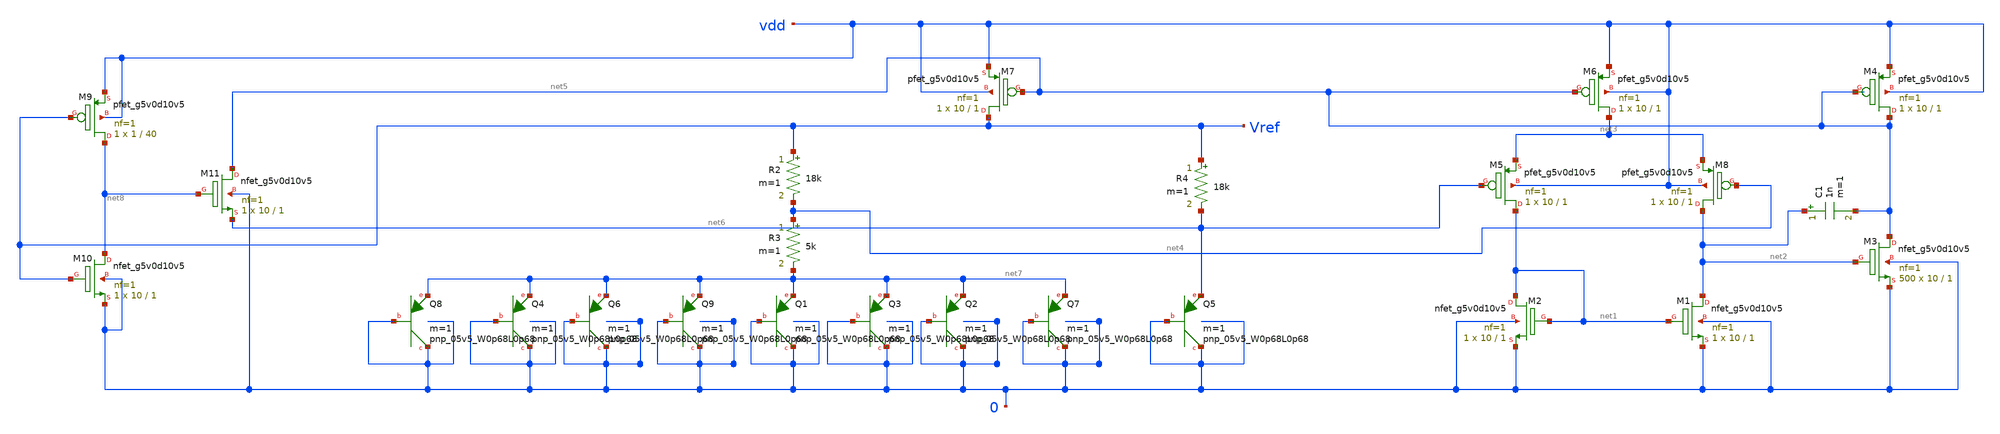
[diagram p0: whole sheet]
** sch_path: Bandgap/My Design/Schematics/Bandgap_opamp.sch
**.subckt Bandgap_opamp
XQ3 0 0 net7 sky130_fd_pr__pnp_05v5_W0p68L0p68 m=1
C1 net2 net5 1n m=1
XQ5 0 0 net6 sky130_fd_pr__pnp_05v5_W0p68L0p68 m=1
R2 Vref net4 18k m=1
R3 net4 net7 5k m=1
R4 Vref net6 18k m=1
XQ9 0 0 net7 sky130_fd_pr__pnp_05v5_W0p68L0p68 m=1
XQ1 0 0 net7 sky130_fd_pr__pnp_05v5_W0p68L0p68 m=1
XQ2 0 0 net7 sky130_fd_pr__pnp_05v5_W0p68L0p68 m=1
XQ4 0 0 net7 sky130_fd_pr__pnp_05v5_W0p68L0p68 m=1
XQ6 0 0 net7 sky130_fd_pr__pnp_05v5_W0p68L0p68 m=1
XQ7 0 0 net7 sky130_fd_pr__pnp_05v5_W0p68L0p68 m=1
XQ8 0 0 net7 sky130_fd_pr__pnp_05v5_W0p68L0p68 m=1
XM1 net2 net1 0 0 sky130_fd_pr__nfet_g5v0d10v5 L=1 W=10 nf=1 ad='int((nf+1)/2) * W/nf * 0.29' as='int((nf+2)/2) * W/nf * 0.29'
+ pd='2*int((nf+1)/2) * (W/nf + 0.29)' ps='2*int((nf+2)/2) * (W/nf + 0.29)' nrd='0.29 / W' nrs='0.29 / W'
+ sa=0 sb=0 sd=0 mult=1 m=1
XM2 net1 net1 0 0 sky130_fd_pr__nfet_g5v0d10v5 L=1 W=10 nf=1 ad='int((nf+1)/2) * W/nf * 0.29' as='int((nf+2)/2) * W/nf * 0.29'
+ pd='2*int((nf+1)/2) * (W/nf + 0.29)' ps='2*int((nf+2)/2) * (W/nf + 0.29)' nrd='0.29 / W' nrs='0.29 / W'
+ sa=0 sb=0 sd=0 mult=1 m=1
XM3 net5 net2 0 0 sky130_fd_pr__nfet_g5v0d10v5 L=1 W=10 nf=1 ad='int((nf+1)/2) * W/nf * 0.29' as='int((nf+2)/2) * W/nf * 0.29'
+ pd='2*int((nf+1)/2) * (W/nf + 0.29)' ps='2*int((nf+2)/2) * (W/nf + 0.29)' nrd='0.29 / W' nrs='0.29 / W'
+ sa=0 sb=0 sd=0 mult=500 m=500
XM4 net5 net5 vdd vdd sky130_fd_pr__pfet_g5v0d10v5 L=1 W=10 nf=1 ad='int((nf+1)/2) * W/nf * 0.29' as='int((nf+2)/2) * W/nf * 0.29'
+ pd='2*int((nf+1)/2) * (W/nf + 0.29)' ps='2*int((nf+2)/2) * (W/nf + 0.29)' nrd='0.29 / W' nrs='0.29 / W'
+ sa=0 sb=0 sd=0 mult=1 m=1
XM5 net1 net6 net3 vdd sky130_fd_pr__pfet_g5v0d10v5 L=1 W=10 nf=1 ad='int((nf+1)/2) * W/nf * 0.29' as='int((nf+2)/2) * W/nf * 0.29'
+ pd='2*int((nf+1)/2) * (W/nf + 0.29)' ps='2*int((nf+2)/2) * (W/nf + 0.29)' nrd='0.29 / W' nrs='0.29 / W'
+ sa=0 sb=0 sd=0 mult=1 m=1
XM6 net3 net5 vdd vdd sky130_fd_pr__pfet_g5v0d10v5 L=1 W=10 nf=1 ad='int((nf+1)/2) * W/nf * 0.29' as='int((nf+2)/2) * W/nf * 0.29'
+ pd='2*int((nf+1)/2) * (W/nf + 0.29)' ps='2*int((nf+2)/2) * (W/nf + 0.29)' nrd='0.29 / W' nrs='0.29 / W'
+ sa=0 sb=0 sd=0 mult=1 m=1
XM7 Vref net5 vdd vdd sky130_fd_pr__pfet_g5v0d10v5 L=1 W=10 nf=1 ad='int((nf+1)/2) * W/nf * 0.29' as='int((nf+2)/2) * W/nf * 0.29'
+ pd='2*int((nf+1)/2) * (W/nf + 0.29)' ps='2*int((nf+2)/2) * (W/nf + 0.29)' nrd='0.29 / W' nrs='0.29 / W'
+ sa=0 sb=0 sd=0 mult=1 m=1
XM8 net2 net4 net3 vdd sky130_fd_pr__pfet_g5v0d10v5 L=1 W=10 nf=1 ad='int((nf+1)/2) * W/nf * 0.29' as='int((nf+2)/2) * W/nf * 0.29'
+ pd='2*int((nf+1)/2) * (W/nf + 0.29)' ps='2*int((nf+2)/2) * (W/nf + 0.29)' nrd='0.29 / W' nrs='0.29 / W'
+ sa=0 sb=0 sd=0 mult=1 m=1
XM9 net8 Vref vdd vdd sky130_fd_pr__pfet_g5v0d10v5 L=40 W=1 nf=1 ad='int((nf+1)/2) * W/nf * 0.29' as='int((nf+2)/2) * W/nf * 0.29'
+ pd='2*int((nf+1)/2) * (W/nf + 0.29)' ps='2*int((nf+2)/2) * (W/nf + 0.29)' nrd='0.29 / W' nrs='0.29 / W'
+ sa=0 sb=0 sd=0 mult=1 m=1
XM10 net8 Vref 0 0 sky130_fd_pr__nfet_g5v0d10v5 L=1 W=10 nf=1 ad='int((nf+1)/2) * W/nf * 0.29' as='int((nf+2)/2) * W/nf * 0.29'
+ pd='2*int((nf+1)/2) * (W/nf + 0.29)' ps='2*int((nf+2)/2) * (W/nf + 0.29)' nrd='0.29 / W' nrs='0.29 / W'
+ sa=0 sb=0 sd=0 mult=1 m=1
XM11 net5 net8 net6 0 sky130_fd_pr__nfet_g5v0d10v5 L=1 W=10 nf=1 ad='int((nf+1)/2) * W/nf * 0.29' as='int((nf+2)/2) * W/nf * 0.29'
+ pd='2*int((nf+1)/2) * (W/nf + 0.29)' ps='2*int((nf+2)/2) * (W/nf + 0.29)' nrd='0.29 / W' nrs='0.29 / W'
+ sa=0 sb=0 sd=0 mult=1 m=1
**** begin user architecture code

.include $::SKYWATER_MODELS/cells/nfet_01v8/sky130_fd_pr__nfet_01v8__tt.corner.spice
.include $::SKYWATER_MODELS/cells/nfet_01v8_lvt/sky130_fd_pr__nfet_01v8_lvt__tt.corner.spice
.include $::SKYWATER_MODELS/cells/pfet_01v8/sky130_fd_pr__pfet_01v8__tt.corner.spice
.include $::SKYWATER_MODELS/cells/nfet_03v3_nvt/sky130_fd_pr__nfet_03v3_nvt__tt.corner.spice
.include $::SKYWATER_MODELS/cells/nfet_05v0_nvt/sky130_fd_pr__nfet_05v0_nvt__tt.corner.spice
.include $::SKYWATER_MODELS/cells/esd_nfet_01v8/sky130_fd_pr__esd_nfet_01v8__tt.corner.spice
.include $::SKYWATER_MODELS/cells/pfet_01v8_lvt/sky130_fd_pr__pfet_01v8_lvt__tt.corner.spice
.include $::SKYWATER_MODELS/cells/pfet_01v8_hvt/sky130_fd_pr__pfet_01v8_hvt__tt.corner.spice
.include $::SKYWATER_MODELS/cells/esd_pfet_g5v0d10v5/sky130_fd_pr__esd_pfet_g5v0d10v5__tt.corner.spice
.include $::SKYWATER_MODELS/cells/pfet_g5v0d10v5/sky130_fd_pr__pfet_g5v0d10v5__tt.corner.spice
.include $::SKYWATER_MODELS/cells/pfet_g5v0d16v0/sky130_fd_pr__pfet_g5v0d16v0__tt.corner.spice
.include $::SKYWATER_MODELS/cells/nfet_g5v0d10v5/sky130_fd_pr__nfet_g5v0d10v5__tt.corner.spice
.include $::SKYWATER_MODELS/cells/nfet_g5v0d16v0/sky130_fd_pr__nfet_g5v0d16v0__tt_discrete.corner.spice
.include $::SKYWATER_MODELS/cells/esd_nfet_g5v0d10v5/sky130_fd_pr__esd_nfet_g5v0d10v5__tt.corner.spice
.include $::SKYWATER_MODELS/models/corners/tt/nonfet.spice
* Mismatch parameters
.include $::SKYWATER_MODELS/cells/nfet_01v8/sky130_fd_pr__nfet_01v8__mismatch.corner.spice
.include $::SKYWATER_MODELS/cells/pfet_01v8/sky130_fd_pr__pfet_01v8__mismatch.corner.spice
.include $::SKYWATER_MODELS/cells/nfet_01v8_lvt/sky130_fd_pr__nfet_01v8_lvt__mismatch.corner.spice
.include $::SKYWATER_MODELS/cells/pfet_01v8_lvt/sky130_fd_pr__pfet_01v8_lvt__mismatch.corner.spice
.include $::SKYWATER_MODELS/cells/pfet_01v8_hvt/sky130_fd_pr__pfet_01v8_hvt__mismatch.corner.spice
.include $::SKYWATER_MODELS/cells/nfet_g5v0d10v5/sky130_fd_pr__nfet_g5v0d10v5__mismatch.corner.spice
.include $::SKYWATER_MODELS/cells/pfet_g5v0d10v5/sky130_fd_pr__pfet_g5v0d10v5__mismatch.corner.spice
.include $::SKYWATER_MODELS/cells/nfet_05v0_nvt/sky130_fd_pr__nfet_05v0_nvt__mismatch.corner.spice
.include $::SKYWATER_MODELS/cells/nfet_03v3_nvt/sky130_fd_pr__nfet_03v3_nvt__mismatch.corner.spice
* Resistor$::SKYWATER_MODELS/Capacitor
.include $::SKYWATER_MODELS/models/r+c/res_typical__cap_typical.spice
.include $::SKYWATER_MODELS/models/r+c/res_typical__cap_typical__lin.spice
* Special cells
.include $::SKYWATER_MODELS/models/corners/tt/specialized_cells.spice
* All models
.include $::SKYWATER_MODELS/models/all.spice
* Corner
.include $::SKYWATER_MODELS/models/corners/tt/rf.spice



*vin vdd 0 dc 0 pwl(0 0 100u 0 200u 5 500u 5)
*.tran 100u 500u
vin vdd 0 3.3
.DC TEMP -40 125 10
*.DC vin 0 5 0.5
.end


**** end user architecture code
**.ends
.end
